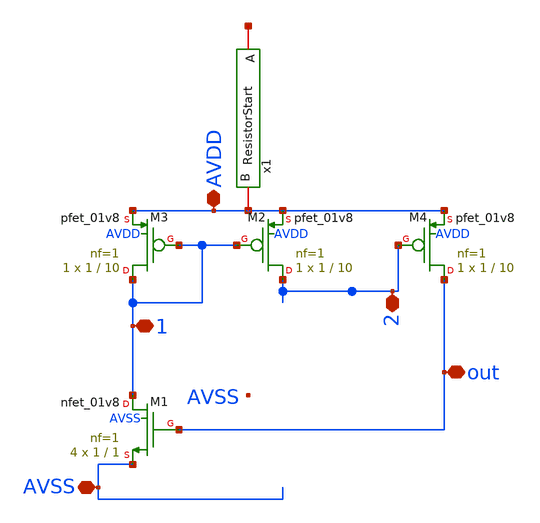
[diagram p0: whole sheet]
** sch_path: xschem/Startup.sch
**.subckt Startup AVDD AVSS out 1 2
*.iopin AVDD
*.iopin AVSS
*.iopin out
*.iopin 1
*.iopin 2
XM1 1 out AVSS AVSS sky130_fd_pr__nfet_01v8 L=1 W=1 nf=1 ad='int((nf+1)/2) * W/nf * 0.29' as='int((nf+2)/2) * W/nf * 0.29'
+ pd='2*int((nf+1)/2) * (W/nf + 0.29)' ps='2*int((nf+2)/2) * (W/nf + 0.29)' nrd='0.29 / W' nrs='0.29 / W'
+ sa=0 sb=0 sd=0 mult=4 m=4
XM2 2 1 AVDD AVDD sky130_fd_pr__pfet_01v8 L=10 W=1 nf=1 ad='int((nf+1)/2) * W/nf * 0.29' as='int((nf+2)/2) * W/nf * 0.29'
+ pd='2*int((nf+1)/2) * (W/nf + 0.29)' ps='2*int((nf+2)/2) * (W/nf + 0.29)' nrd='0.29 / W' nrs='0.29 / W'
+ sa=0 sb=0 sd=0 mult=1 m=1
XM3 1 1 AVDD AVDD sky130_fd_pr__pfet_01v8 L=10 W=1 nf=1 ad='int((nf+1)/2) * W/nf * 0.29' as='int((nf+2)/2) * W/nf * 0.29'
+ pd='2*int((nf+1)/2) * (W/nf + 0.29)' ps='2*int((nf+2)/2) * (W/nf + 0.29)' nrd='0.29 / W' nrs='0.29 / W'
+ sa=0 sb=0 sd=0 mult=1 m=1
XM4 out 2 AVDD AVDD sky130_fd_pr__pfet_01v8 L=10 W=1 nf=1 ad='int((nf+1)/2) * W/nf * 0.29' as='int((nf+2)/2) * W/nf * 0.29'
+ pd='2*int((nf+1)/2) * (W/nf + 0.29)' ps='2*int((nf+2)/2) * (W/nf + 0.29)' nrd='0.29 / W' nrs='0.29 / W'
+ sa=0 sb=0 sd=0 mult=1 m=1
x1 AVDD net1 ResistorStart
**.ends

* expanding   symbol:  ResistorStart.sym # of pins=2
** sym_path: xschem/ResistorStart.sym
** sch_path: xschem/ResistorStart.sch
.subckt ResistorStart B A
*.iopin A
*.iopin B
XR1 net1 A GND sky130_fd_pr__res_high_po_0p35 L=17 mult=1 m=1
XR2 net2 net1 GND sky130_fd_pr__res_high_po_0p35 L={L} mult=1 m=1
XR3 net4 net2 GND sky130_fd_pr__res_high_po_0p35 L={L} mult=1 m=1
XR4 net3 net4 GND sky130_fd_pr__res_high_po_0p35 L={L} mult=1 m=1
XR5 net5 net3 GND sky130_fd_pr__res_high_po_0p35 L={L} mult=1 m=1
**** begin user architecture code


.param L=17


**** end user architecture code
XR6 net6 net7 GND sky130_fd_pr__res_high_po_0p35 L={L} mult=1 m=1
XR7 net8 net6 GND sky130_fd_pr__res_high_po_0p35 L={L} mult=1 m=1
XR8 net10 net8 GND sky130_fd_pr__res_high_po_0p35 L={L} mult=1 m=1
XR9 net9 net10 GND sky130_fd_pr__res_high_po_0p35 L={L} mult=1 m=1
XR10 net5 net9 GND sky130_fd_pr__res_high_po_0p35 L={L} mult=1 m=1
XR11 net11 net7 GND sky130_fd_pr__res_high_po_0p35 L={L} mult=1 m=1
XR12 net12 net11 GND sky130_fd_pr__res_high_po_0p35 L={L} mult=1 m=1
XR13 net14 net12 GND sky130_fd_pr__res_high_po_0p35 L={L} mult=1 m=1
XR14 net13 net14 GND sky130_fd_pr__res_high_po_0p35 L={L} mult=1 m=1
XR15 net15 net13 GND sky130_fd_pr__res_high_po_0p35 L={L} mult=1 m=1
XR16 net16 net17 GND sky130_fd_pr__res_high_po_0p35 L={L} mult=1 m=1
XR17 net18 net16 GND sky130_fd_pr__res_high_po_0p35 L={L} mult=1 m=1
XR18 net20 net18 GND sky130_fd_pr__res_high_po_0p35 L={L} mult=1 m=1
XR19 net19 net20 GND sky130_fd_pr__res_high_po_0p35 L={L} mult=1 m=1
XR20 net15 net19 GND sky130_fd_pr__res_high_po_0p35 L={L} mult=1 m=1
XR21 net21 net17 GND sky130_fd_pr__res_high_po_0p35 L={L} mult=1 m=1
XR22 net22 net21 GND sky130_fd_pr__res_high_po_0p35 L={L} mult=1 m=1
XR23 net23 net22 GND sky130_fd_pr__res_high_po_0p35 L={L} mult=1 m=1
XR24 net24 net23 GND sky130_fd_pr__res_high_po_0p35 L={L} mult=1 m=1
XR25 net25 net24 GND sky130_fd_pr__res_high_po_0p35 L={L} mult=1 m=1
XR26 net26 B GND sky130_fd_pr__res_high_po_0p35 L={L} mult=1 m=1
XR27 net27 net26 GND sky130_fd_pr__res_high_po_0p35 L={L} mult=1 m=1
XR28 net28 net27 GND sky130_fd_pr__res_high_po_0p35 L={L} mult=1 m=1
XR29 net29 net28 GND sky130_fd_pr__res_high_po_0p35 L={L} mult=1 m=1
XR30 net25 net29 GND sky130_fd_pr__res_high_po_0p35 L={L} mult=1 m=1
.ends

.GLOBAL GND
.end
